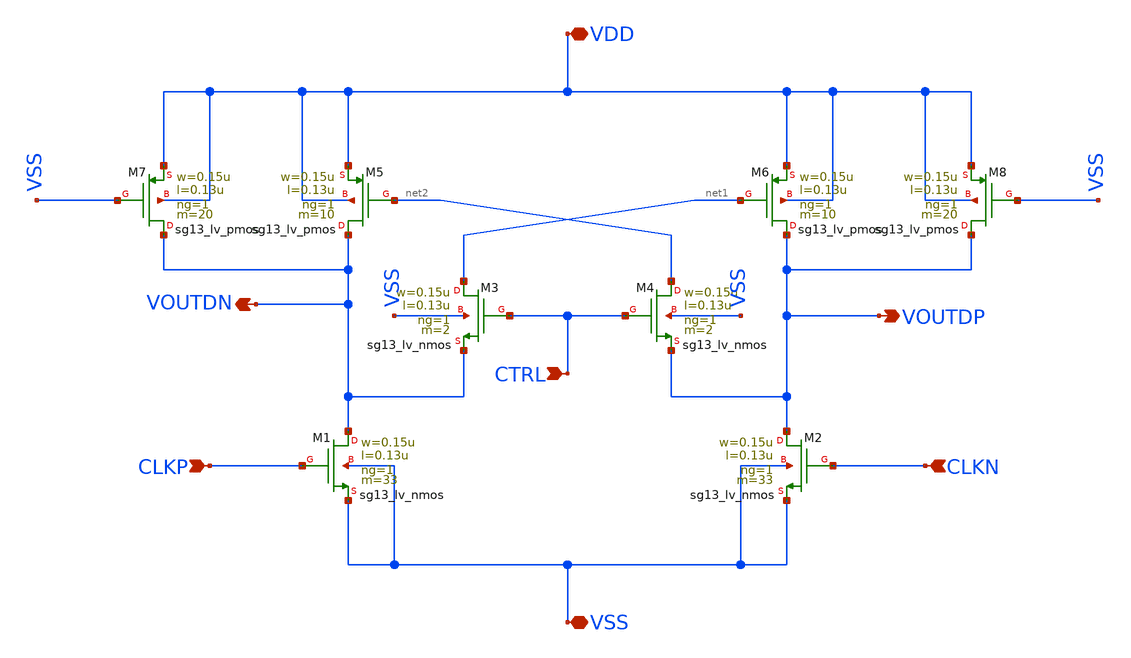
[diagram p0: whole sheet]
** sch_path: 2to4/2to4_psdiff.sch
**.subckt 2to4_psdiff VSS CLKP CLKN VDD CTRL VOUTDN VOUTDP
*.iopin VSS
*.ipin CLKP
*.ipin CLKN
*.iopin VDD
*.ipin CTRL
*.opin VOUTDN
*.opin VOUTDP
XM1 VOUTDN CLKP VSS VSS sg13_lv_nmos w=0.15u l=0.13u ng=1 m=33 mm_ok=1
XM2 VOUTDP CLKN VSS VSS sg13_lv_nmos w=0.15u l=0.13u ng=1 m=33 mm_ok=1
XM3 net1 CTRL VOUTDN VSS sg13_lv_nmos w=0.15u l=0.13u ng=1 m=2 mm_ok=1
XM4 net2 CTRL VOUTDP VSS sg13_lv_nmos w=0.15u l=0.13u ng=1 m=2 mm_ok=1
XM6 VOUTDP net1 VDD VDD sg13_lv_pmos w=0.15u l=0.13u ng=1 m=10 mm_ok=1
XM5 VOUTDN net2 VDD VDD sg13_lv_pmos w=0.15u l=0.13u ng=1 m=10 mm_ok=1
XM7 VOUTDN VSS VDD VDD sg13_lv_pmos w=0.15u l=0.13u ng=1 m=20 mm_ok=1
XM8 VOUTDP VSS VDD VDD sg13_lv_pmos w=0.15u l=0.13u ng=1 m=20 mm_ok=1
**.ends
.end
